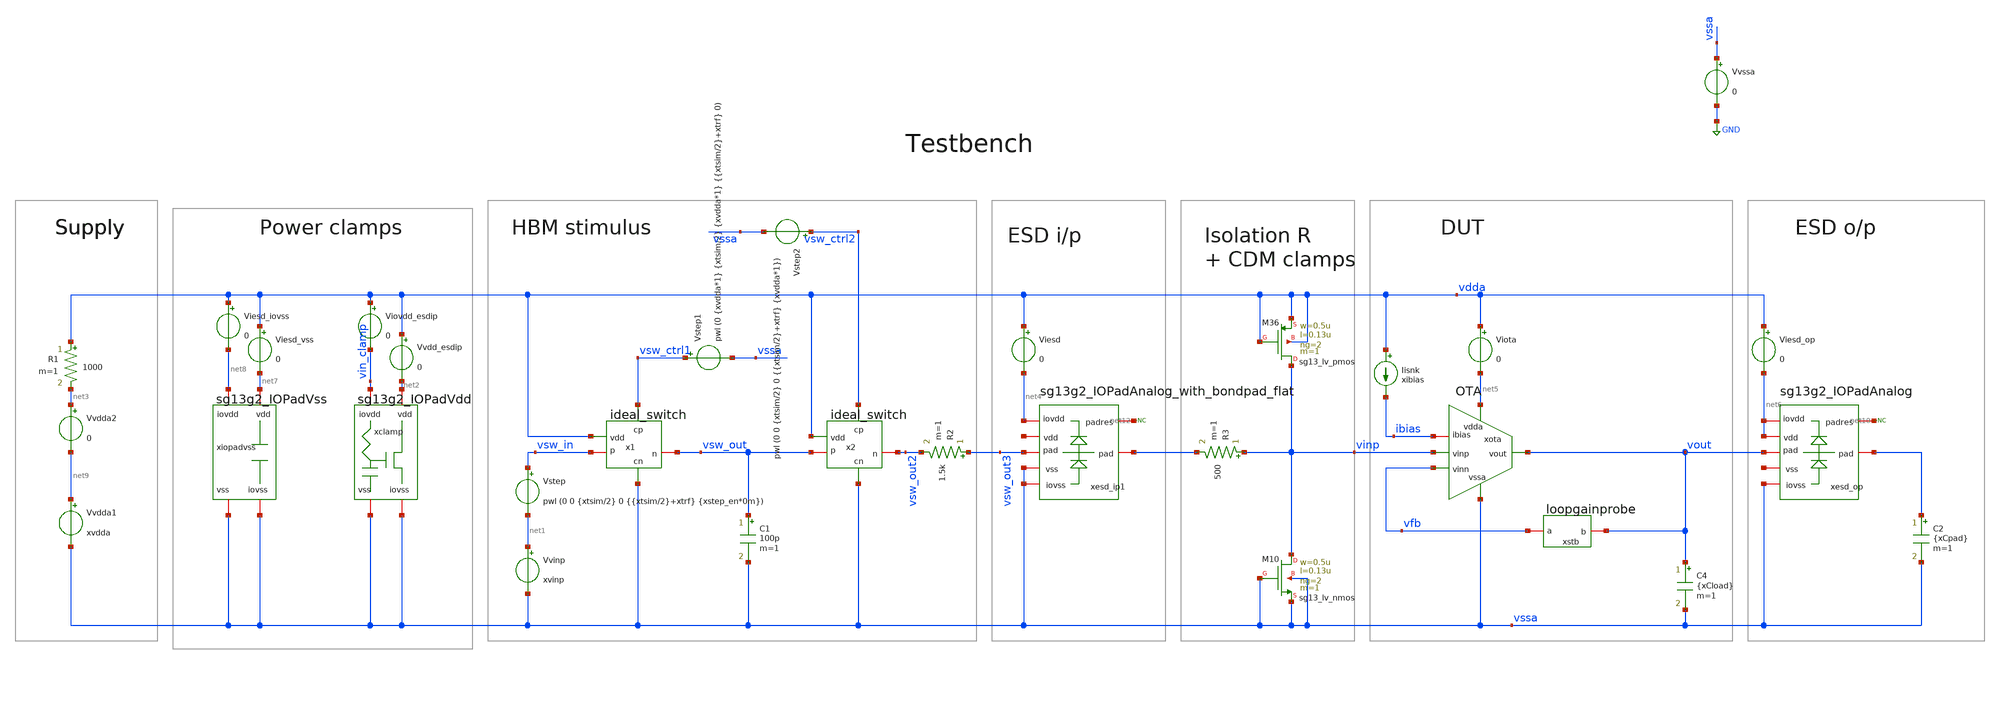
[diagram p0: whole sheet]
** sch_path: tb_OTA_1stage_ihp/tb_OTA_esd.sch
**.subckt tb_OTA_esd
Iisnk vdda ibias xibias
xota net5 vinp vfb vssa vout ibias OTA
Vstep vsw_in net1 pwl (0 0 {xtsim/2} 0 {{xtsim/2}+xtrf} {xstep_en*0m})
Vvinp net1 vssa xvinp
Vvssa vssa GND 0
xstb vfb vout loopgainprobe
xclamp vin_clamp vssa net2 vssa sg13g2_IOPadVdd
xiopadvss net8 vssa net7 vssa sg13g2_IOPadVss
xesd_op net6 vssa net10 net6 vout net11 sg13g2_IOPadAnalog
C2 vout vssa {xCpad} m=1
* noconn #net10
C4 vout vssa {xCload} m=1
R1 vdda net3 1000 m=1
Vvdda1 net9 vssa xvdda
Vvdd_esdip vdda net2 0
Viovdd_esdip vdda vin_clamp 0
Vvdda2 net3 net9 0
Viesd vdda net4 0
Viota vdda net5 0
Viesd_op vdda net6 0
Viesd_vss vdda net7 0
Viesd_iovss vdda net8 0
C1 vsw_out vssa 100p m=1
R2 vsw_out3 vsw_out2 1.5k m=1
x1 vdda vsw_ctrl1 vsw_in vsw_out vssa ideal_switch
Vstep1 vsw_ctrl1 vssa pwl (0 {xvdda*1} {xtsim/2} {xvdda*1} {{xtsim/2}+xtrf} 0)
x2 vdda vsw_ctrl2 vsw_out vsw_out2 vssa ideal_switch
Vstep2 vsw_ctrl2 vssa pwl (0 0 {xtsim/2} 0 {{xtsim/2}+xtrf} {xvdda*1})
* noconn #net12
XM10 vinp vssa vssa vssa sg13_lv_nmos w=0.5u l=0.13u ng=2 m=1 mm_ok=1
XM36 vinp vdda vdda vdda sg13_lv_pmos w=0.5u l=0.13u ng=2 m=1 mm_ok=1
R3 vinp vsw_out3 500 m=1
xesd_ip1 net4 vssa net12 net13 vsw_out3 vssa sg13g2_IOPadAnalog_with_bondpad_flat
**** begin user architecture code

** opencircuitdesign pdks install
.lib /home/slice/pdk/iHP/IHP-Open-PDK/ihp-sg13g2/libs.tech/ngspice/models/cornerMOSlv.lib mos_tt
*.lib /home/slice/pdk/iHP/IHP-Open-PDK/ihp-sg13g2/libs.tech/ngspice/models/sg13g2_moshv_mod.lib
.lib /home/slice/pdk/iHP/IHP-Open-PDK/ihp-sg13g2/libs.tech/ngspice/models/cornerMOShv.lib mos_tt
.lib /home/slice/pdk/iHP/IHP-Open-PDK/ihp-sg13g2/libs.tech/ngspice/models/cornerRES.lib res_typ
.include /home/slice/pdk/iHP/IHP-Open-PDK/ihp-sg13g2/libs.tech/ngspice/models/diodes.lib
*.lib /home/slice/xschem/tb_OTA_1stage_ihp/cornerRES.lib res_typ
*.lib /home/slice/xschem/tb_OTA_1stage_ihp/resistors_mod.lib

*.model
*+ /home/slice/pdk/iHP/IHP-Open-PDK/ihp-sg13g2/libs.tech/ngspice/models/sg13g2_moshv_mod.lib/sg13_hv_pmos

*.model /home/slice/Desktop/acm2/MOSFET_model/Verilog-A/NMOS_ACM_2V0.va
*.model /home/slice/Desktop/acm2/MOSFET_model/Verilog-A/PMOS_ACM_2V0.va

* Parameters
.param xvdda = 1.8
.param xvinp = 2000
.param xibias = 40u
.param xCload = 0.75p
.param xCpad = 100f
.param xgm_dp = 1e-3
.param xRin = 1/xgm_dp
.param xCout = 1p
.param xRout = 1e6
.param xtrf = 1.5n
.param xtsim = 5u
.csparam xtsim_var = 'xtsim'
.param xstep_en = 1

* vlogA instantiation
*.model OTA_vcvs OTA_vcvs
.model ideal_sw ideal_sw


  ** must save the below for DCOP analysis to be back annotated onto the schematic
  .option savecurrents

  .include tb_OTA.save
  *.save all
  .save v(vout) v(vinp) v(vfb) v(vdda) v(xota.pdio) v(xota.vtail) v(vout_pad) v(vin_clamp)
  .save v(vsw_in) v(vsw_out) v(vsw_ctrl1) v(vsw_ctrl2) v(vsw_outs) v(vsw_out2) v(vsw_out3)
  .save i(v.xota.Virhs) i(v.xota.Vitail) i(xota.vdda) i(v.Vdda) i(xesd_ip.pad) i(v.Vstep) i(@r3[i])
  .save i(@n.xota.xm6.nsg13_lv_pmos[ids]) i(@n.xm36.nsg13_lv_pmos[ids]) i(@n.xm10.nsg13_lv_nmos[ids])
  .save @n.xm10.nsg13_lv_nmos[ids] @n.xm36.nsg13_lv_pmos[ids] @n.xm36.nsg13_lv_pmos[idb]


  .control
  let xtsim = $&xtsim_var
*  pre_osdi OTA_vcvs.osdi
  pre_osdi ideal_sw.osdi
  save all

** 1. DCOP ANALYSIS **

  op
  set filetype=ascii
  remzerovec
  write tb_OTA_op.raw

** 2. TRAN ANALYSIS **

  tran 1n $&xtsim
  echo --
  echo TSIM VALUE
    echo $&xtsim
    echo --
  *set filetype=ascii
  remzerovec
  write tb_OTA_tran.raw

** 3. AC ANALYSIS **

  alter i.xstb.Ii acmag=0
  alter v.xstb.Vi acmag=1

  ac dec 10 1 100G

  remzerovec
  write tb_OTA_1stage_ac1.raw

  alter i.xstb.Ii acmag=1
  alter v.xstb.Vi acmag=0

  ac dec 10 1 100G

  * use this line if you want the phase response to start at 180deg
  *let av = {1/(1-1/(2*(ac1.i(v.xstb.Vi)*ac2.v(xstb.x)-ac1.v(xstb.x)*ac2.i(v.xstb.Vi))+ac1.v(xstb.x)+ac2.i(v.xstb.Vi)))}

  * use this line if you want the phase response to start at 0deg (more conventional and directly
+ corresponds to Franks derivation)
  let av = {1/(1/(2*(ac1.i(v.xstb.Vi)*ac2.v(xstb.x)-ac1.v(xstb.x)*ac2.i(v.xstb.Vi))+ac1.v(xstb.x)+ac2.i(v.xstb.Vi))-1)}

  remzerovec
  write tb_OTA_1stage_ac2.raw

  ** 4. MEASURES **

  let n45_rads = -45*(pi/180)
  meas AC Av_0 FIND vdb(av) AT=10
  echo --
  meas AC BW WHEN vp(av)=n45_rads CROSS=1
  echo --
  meas AC Av_BW FIND vdb(av) WHEN vp(av)=n45_rads CROSS=1
  echo --
  meas AC ULGF WHEN vdb(av)=0
  echo --
  meas AC ULGF_phi_rads FIND vp(av) WHEN vdb(av)=0 CROSS=1
  let ULGF_phi_deg = ULGF_phi_rads*(180/pi)
  print ULGF_phi_deg
  let PM = 180+ULGF_phi_deg
  print PM
  echo --
  * putting in -170 since this is a 2nd-order system so doesnt ever achieve -180
  let n180_rads = -170*(pi/180)
  meas AC GM FIND vdb(av) WHEN vp(av)=n180_rads CROSS=1

  setplot
*quit 0
.endc




**** end user architecture code
**.ends
.GLOBAL GND
.end
